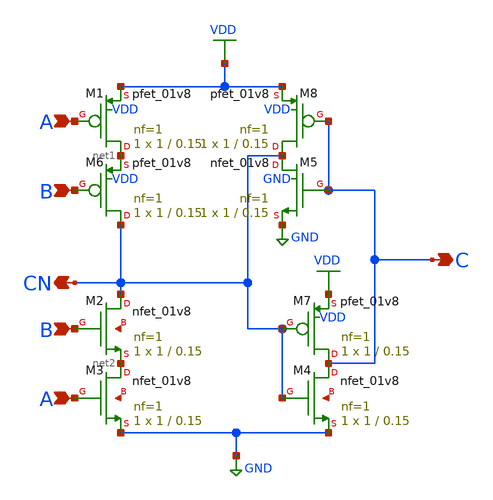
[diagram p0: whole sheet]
** sch_path: cells/xschem/ASYNC2.sch
**.subckt ASYNC2 A B B A CN C
*.ipin A
*.ipin B
*.ipin B
*.ipin A
*.opin CN
*.opin C
XM5 CN C GND GND sky130_fd_pr__nfet_01v8 L=0.15 W=1 nf=1 ad='int((nf+1)/2) * W/nf * 0.29' as='int((nf+2)/2) * W/nf * 0.29'
+ pd='2*int((nf+1)/2) * (W/nf + 0.29)' ps='2*int((nf+2)/2) * (W/nf + 0.29)' nrd='0.29 / W' nrs='0.29 / W'
+ sa=0 sb=0 sd=0 mult=1 m=1
XM1 net1 A VDD VDD sky130_fd_pr__pfet_01v8 L=0.15 W=1 nf=1 ad='int((nf+1)/2) * W/nf * 0.29' as='int((nf+2)/2) * W/nf * 0.29'
+ pd='2*int((nf+1)/2) * (W/nf + 0.29)' ps='2*int((nf+2)/2) * (W/nf + 0.29)' nrd='0.29 / W' nrs='0.29 / W'
+ sa=0 sb=0 sd=0 mult=1 m=1
XM6 CN B net1 VDD sky130_fd_pr__pfet_01v8 L=0.15 W=1 nf=1 ad='int((nf+1)/2) * W/nf * 0.29' as='int((nf+2)/2) * W/nf * 0.29'
+ pd='2*int((nf+1)/2) * (W/nf + 0.29)' ps='2*int((nf+2)/2) * (W/nf + 0.29)' nrd='0.29 / W' nrs='0.29 / W'
+ sa=0 sb=0 sd=0 mult=1 m=1
XM7 C CN VDD VDD sky130_fd_pr__pfet_01v8 L=0.15 W=1 nf=1 ad='int((nf+1)/2) * W/nf * 0.29' as='int((nf+2)/2) * W/nf * 0.29'
+ pd='2*int((nf+1)/2) * (W/nf + 0.29)' ps='2*int((nf+2)/2) * (W/nf + 0.29)' nrd='0.29 / W' nrs='0.29 / W'
+ sa=0 sb=0 sd=0 mult=1 m=1
XM8 CN C VDD VDD sky130_fd_pr__pfet_01v8 L=0.15 W=1 nf=1 ad='int((nf+1)/2) * W/nf * 0.29' as='int((nf+2)/2) * W/nf * 0.29'
+ pd='2*int((nf+1)/2) * (W/nf + 0.29)' ps='2*int((nf+2)/2) * (W/nf + 0.29)' nrd='0.29 / W' nrs='0.29 / W'
+ sa=0 sb=0 sd=0 mult=1 m=1
XM2 CN B net2 net3 sky130_fd_pr__nfet_01v8 L=0.15 W=1 nf=1 ad='int((nf+1)/2) * W/nf * 0.29' as='int((nf+2)/2) * W/nf * 0.29'
+ pd='2*int((nf+1)/2) * (W/nf + 0.29)' ps='2*int((nf+2)/2) * (W/nf + 0.29)' nrd='0.29 / W' nrs='0.29 / W'
+ sa=0 sb=0 sd=0 mult=1 m=1
XM3 net2 A GND net4 sky130_fd_pr__nfet_01v8 L=0.15 W=1 nf=1 ad='int((nf+1)/2) * W/nf * 0.29' as='int((nf+2)/2) * W/nf * 0.29'
+ pd='2*int((nf+1)/2) * (W/nf + 0.29)' ps='2*int((nf+2)/2) * (W/nf + 0.29)' nrd='0.29 / W' nrs='0.29 / W'
+ sa=0 sb=0 sd=0 mult=1 m=1
XM4 C CN GND net5 sky130_fd_pr__nfet_01v8 L=0.15 W=1 nf=1 ad='int((nf+1)/2) * W/nf * 0.29' as='int((nf+2)/2) * W/nf * 0.29'
+ pd='2*int((nf+1)/2) * (W/nf + 0.29)' ps='2*int((nf+2)/2) * (W/nf + 0.29)' nrd='0.29 / W' nrs='0.29 / W'
+ sa=0 sb=0 sd=0 mult=1 m=1
**.ends
.GLOBAL VDD
.GLOBAL GND
.end
